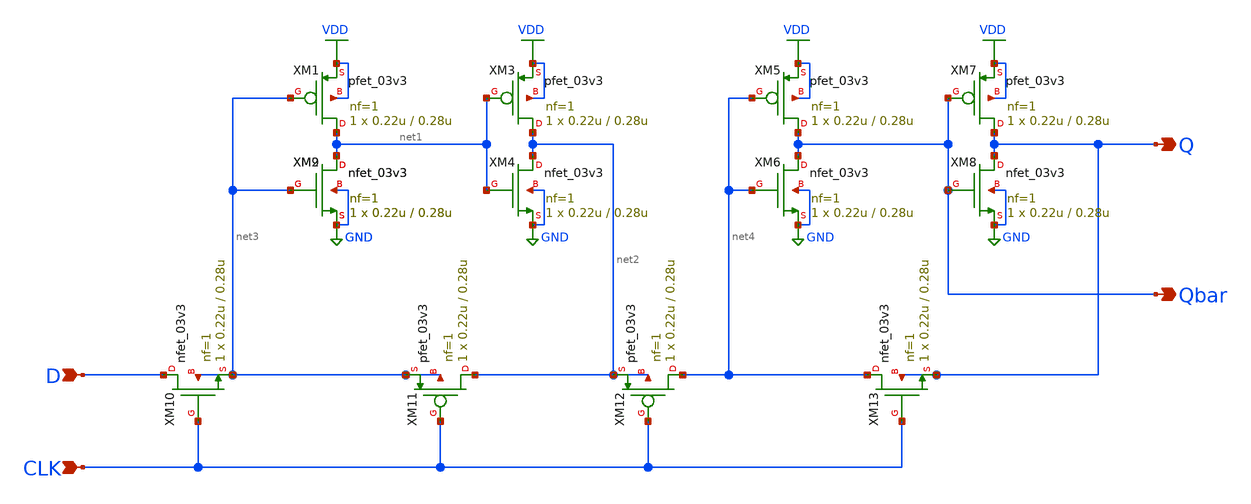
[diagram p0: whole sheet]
** sch_path: Project/1-on-chip/schematic/PNgen/dff.sch
**.subckt dff Qbar CLK D Q
*.opin Qbar
*.ipin CLK
*.ipin D
*.opin Q
XM1 net1 net3 VDD VDD pfet_03v3 L=0.28u W=0.22u nf=1 ad='int((nf+1)/2) * W/nf * 0.18u' as='int((nf+2)/2) * W/nf * 0.18u'
+ pd='2*int((nf+1)/2) * (W/nf + 0.18u)' ps='2*int((nf+2)/2) * (W/nf + 0.18u)' nrd='0.18u / W' nrs='0.18u / W'
+ sa=0 sb=0 sd=0 m=1
XM2 net1 net3 GND GND nfet_03v3 L=0.28u W=0.22u nf=1 ad='int((nf+1)/2) * W/nf * 0.18u' as='int((nf+2)/2) * W/nf * 0.18u'
+ pd='2*int((nf+1)/2) * (W/nf + 0.18u)' ps='2*int((nf+2)/2) * (W/nf + 0.18u)' nrd='0.18u / W' nrs='0.18u / W'
+ sa=0 sb=0 sd=0 m=1
XM3 net2 net1 VDD VDD pfet_03v3 L=0.28u W=0.22u nf=1 ad='int((nf+1)/2) * W/nf * 0.18u' as='int((nf+2)/2) * W/nf * 0.18u'
+ pd='2*int((nf+1)/2) * (W/nf + 0.18u)' ps='2*int((nf+2)/2) * (W/nf + 0.18u)' nrd='0.18u / W' nrs='0.18u / W'
+ sa=0 sb=0 sd=0 m=1
XM4 net2 net1 GND GND nfet_03v3 L=0.28u W=0.22u nf=1 ad='int((nf+1)/2) * W/nf * 0.18u' as='int((nf+2)/2) * W/nf * 0.18u'
+ pd='2*int((nf+1)/2) * (W/nf + 0.18u)' ps='2*int((nf+2)/2) * (W/nf + 0.18u)' nrd='0.18u / W' nrs='0.18u / W'
+ sa=0 sb=0 sd=0 m=1
XM5 Qbar net4 VDD VDD pfet_03v3 L=0.28u W=0.22u nf=1 ad='int((nf+1)/2) * W/nf * 0.18u' as='int((nf+2)/2) * W/nf * 0.18u'
+ pd='2*int((nf+1)/2) * (W/nf + 0.18u)' ps='2*int((nf+2)/2) * (W/nf + 0.18u)' nrd='0.18u / W' nrs='0.18u / W'
+ sa=0 sb=0 sd=0 m=1
XM6 Qbar net4 GND GND nfet_03v3 L=0.28u W=0.22u nf=1 ad='int((nf+1)/2) * W/nf * 0.18u' as='int((nf+2)/2) * W/nf * 0.18u'
+ pd='2*int((nf+1)/2) * (W/nf + 0.18u)' ps='2*int((nf+2)/2) * (W/nf + 0.18u)' nrd='0.18u / W' nrs='0.18u / W'
+ sa=0 sb=0 sd=0 m=1
XM7 Q Qbar VDD VDD pfet_03v3 L=0.28u W=0.22u nf=1 ad='int((nf+1)/2) * W/nf * 0.18u' as='int((nf+2)/2) * W/nf * 0.18u'
+ pd='2*int((nf+1)/2) * (W/nf + 0.18u)' ps='2*int((nf+2)/2) * (W/nf + 0.18u)' nrd='0.18u / W' nrs='0.18u / W'
+ sa=0 sb=0 sd=0 m=1
XM8 Q Qbar GND GND nfet_03v3 L=0.28u W=0.22u nf=1 ad='int((nf+1)/2) * W/nf * 0.18u' as='int((nf+2)/2) * W/nf * 0.18u'
+ pd='2*int((nf+1)/2) * (W/nf + 0.18u)' ps='2*int((nf+2)/2) * (W/nf + 0.18u)' nrd='0.18u / W' nrs='0.18u / W'
+ sa=0 sb=0 sd=0 m=1
XM9 net1 net3 GND GND nfet_03v3 L=0.28u W=0.22u nf=1 ad='int((nf+1)/2) * W/nf * 0.18u' as='int((nf+2)/2) * W/nf * 0.18u'
+ pd='2*int((nf+1)/2) * (W/nf + 0.18u)' ps='2*int((nf+2)/2) * (W/nf + 0.18u)' nrd='0.18u / W' nrs='0.18u / W'
+ sa=0 sb=0 sd=0 m=1
XM10 D CLK net3 net3 nfet_03v3 L=0.28u W=0.22u nf=1 ad='int((nf+1)/2) * W/nf * 0.18u' as='int((nf+2)/2) * W/nf * 0.18u'
+ pd='2*int((nf+1)/2) * (W/nf + 0.18u)' ps='2*int((nf+2)/2) * (W/nf + 0.18u)' nrd='0.18u / W' nrs='0.18u / W'
+ sa=0 sb=0 sd=0 m=1
XM11 net2 CLK net3 net3 pfet_03v3 L=0.28u W=0.22u nf=1 ad='int((nf+1)/2) * W/nf * 0.18u' as='int((nf+2)/2) * W/nf * 0.18u'
+ pd='2*int((nf+1)/2) * (W/nf + 0.18u)' ps='2*int((nf+2)/2) * (W/nf + 0.18u)' nrd='0.18u / W' nrs='0.18u / W'
+ sa=0 sb=0 sd=0 m=1
XM12 net4 CLK net2 net2 pfet_03v3 L=0.28u W=0.22u nf=1 ad='int((nf+1)/2) * W/nf * 0.18u' as='int((nf+2)/2) * W/nf * 0.18u'
+ pd='2*int((nf+1)/2) * (W/nf + 0.18u)' ps='2*int((nf+2)/2) * (W/nf + 0.18u)' nrd='0.18u / W' nrs='0.18u / W'
+ sa=0 sb=0 sd=0 m=1
XM13 net4 CLK Q Q nfet_03v3 L=0.28u W=0.22u nf=1 ad='int((nf+1)/2) * W/nf * 0.18u' as='int((nf+2)/2) * W/nf * 0.18u'
+ pd='2*int((nf+1)/2) * (W/nf + 0.18u)' ps='2*int((nf+2)/2) * (W/nf + 0.18u)' nrd='0.18u / W' nrs='0.18u / W'
+ sa=0 sb=0 sd=0 m=1
**.ends
.GLOBAL GND
.GLOBAL VDD
.end
